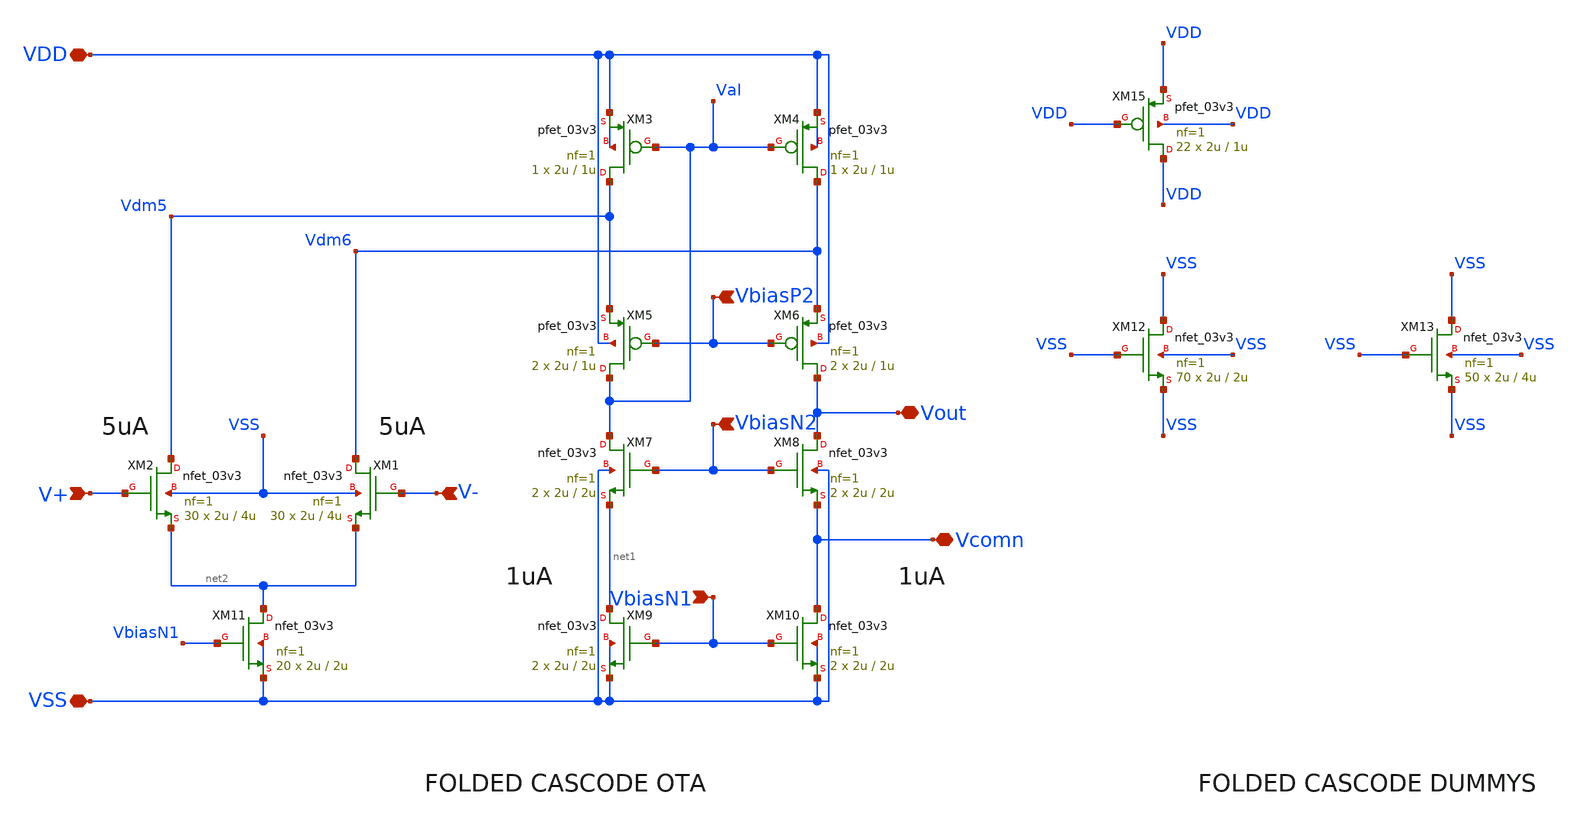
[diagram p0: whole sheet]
** sch_path: designs/libs/error_amplifier_N_input_core_v4/xschem/error_amplifier_N_input_core_v4.sch
**.subckt error_amplifier_N_input_core_v4 VbiasN2 VDD VbiasP2 VbiasN1 V+ V- VSS Vcomn Vout
*.ipin VbiasN2
*.iopin VDD
*.ipin VbiasP2
*.ipin VbiasN1
*.ipin V+
*.ipin V-
*.iopin VSS
*.iopin Vcomn
*.iopin Vout
XM4 Vdm6 Val VDD VDD pfet_03v3 L=1u W=2u nf=1 ad='int((nf+1)/2) * W/nf * 0.18u' as='int((nf+2)/2) * W/nf * 0.18u'
+ pd='2*int((nf+1)/2) * (W/nf + 0.18u)' ps='2*int((nf+2)/2) * (W/nf + 0.18u)' nrd='0.18u / W' nrs='0.18u / W'
+ sa=0 sb=0 sd=0 m=1
XM3 Vdm5 Val VDD VDD pfet_03v3 L=1u W=2u nf=1 ad='int((nf+1)/2) * W/nf * 0.18u' as='int((nf+2)/2) * W/nf * 0.18u'
+ pd='2*int((nf+1)/2) * (W/nf + 0.18u)' ps='2*int((nf+2)/2) * (W/nf + 0.18u)' nrd='0.18u / W' nrs='0.18u / W'
+ sa=0 sb=0 sd=0 m=1
XM5 Val VbiasP2 Vdm5 VDD pfet_03v3 L=1u W=2u nf=1 ad='int((nf+1)/2) * W/nf * 0.18u' as='int((nf+2)/2) * W/nf * 0.18u'
+ pd='2*int((nf+1)/2) * (W/nf + 0.18u)' ps='2*int((nf+2)/2) * (W/nf + 0.18u)' nrd='0.18u / W' nrs='0.18u / W'
+ sa=0 sb=0 sd=0 m=2
XM6 Vout VbiasP2 Vdm6 VDD pfet_03v3 L=1u W=2u nf=1 ad='int((nf+1)/2) * W/nf * 0.18u' as='int((nf+2)/2) * W/nf * 0.18u'
+ pd='2*int((nf+1)/2) * (W/nf + 0.18u)' ps='2*int((nf+2)/2) * (W/nf + 0.18u)' nrd='0.18u / W' nrs='0.18u / W'
+ sa=0 sb=0 sd=0 m=2
XM9 net1 VbiasN1 VSS VSS nfet_03v3 L=2u W=2u nf=1 ad='int((nf+1)/2) * W/nf * 0.18u' as='int((nf+2)/2) * W/nf * 0.18u'
+ pd='2*int((nf+1)/2) * (W/nf + 0.18u)' ps='2*int((nf+2)/2) * (W/nf + 0.18u)' nrd='0.18u / W' nrs='0.18u / W'
+ sa=0 sb=0 sd=0 m=2
XM8 Vout VbiasN2 Vcomn VSS nfet_03v3 L=2u W=2u nf=1 ad='int((nf+1)/2) * W/nf * 0.18u' as='int((nf+2)/2) * W/nf * 0.18u'
+ pd='2*int((nf+1)/2) * (W/nf + 0.18u)' ps='2*int((nf+2)/2) * (W/nf + 0.18u)' nrd='0.18u / W' nrs='0.18u / W'
+ sa=0 sb=0 sd=0 m=2
XM7 Val VbiasN2 net1 VSS nfet_03v3 L=2u W=2u nf=1 ad='int((nf+1)/2) * W/nf * 0.18u' as='int((nf+2)/2) * W/nf * 0.18u'
+ pd='2*int((nf+1)/2) * (W/nf + 0.18u)' ps='2*int((nf+2)/2) * (W/nf + 0.18u)' nrd='0.18u / W' nrs='0.18u / W'
+ sa=0 sb=0 sd=0 m=2
XM10 Vcomn VbiasN1 VSS VSS nfet_03v3 L=2u W=2u nf=1 ad='int((nf+1)/2) * W/nf * 0.18u' as='int((nf+2)/2) * W/nf * 0.18u'
+ pd='2*int((nf+1)/2) * (W/nf + 0.18u)' ps='2*int((nf+2)/2) * (W/nf + 0.18u)' nrd='0.18u / W' nrs='0.18u / W'
+ sa=0 sb=0 sd=0 m=2
XM15 VDD VDD VDD VDD pfet_03v3 L=1u W=2u nf=1 ad='int((nf+1)/2) * W/nf * 0.18u' as='int((nf+2)/2) * W/nf * 0.18u'
+ pd='2*int((nf+1)/2) * (W/nf + 0.18u)' ps='2*int((nf+2)/2) * (W/nf + 0.18u)' nrd='0.18u / W' nrs='0.18u / W'
+ sa=0 sb=0 sd=0 m=22
XM13 VSS VSS VSS VSS nfet_03v3 L=4u W=2u nf=1 ad='int((nf+1)/2) * W/nf * 0.18u' as='int((nf+2)/2) * W/nf * 0.18u'
+ pd='2*int((nf+1)/2) * (W/nf + 0.18u)' ps='2*int((nf+2)/2) * (W/nf + 0.18u)' nrd='0.18u / W' nrs='0.18u / W'
+ sa=0 sb=0 sd=0 m=50
XM12 VSS VSS VSS VSS nfet_03v3 L=2u W=2u nf=1 ad='int((nf+1)/2) * W/nf * 0.18u' as='int((nf+2)/2) * W/nf * 0.18u'
+ pd='2*int((nf+1)/2) * (W/nf + 0.18u)' ps='2*int((nf+2)/2) * (W/nf + 0.18u)' nrd='0.18u / W' nrs='0.18u / W'
+ sa=0 sb=0 sd=0 m=70
XM1 Vdm6 V- net2 VSS nfet_03v3 L=4u W=2u nf=1 ad='int((nf+1)/2) * W/nf * 0.18u' as='int((nf+2)/2) * W/nf * 0.18u'
+ pd='2*int((nf+1)/2) * (W/nf + 0.18u)' ps='2*int((nf+2)/2) * (W/nf + 0.18u)' nrd='0.18u / W' nrs='0.18u / W'
+ sa=0 sb=0 sd=0 m=30
XM2 Vdm5 V+ net2 VSS nfet_03v3 L=4u W=2u nf=1 ad='int((nf+1)/2) * W/nf * 0.18u' as='int((nf+2)/2) * W/nf * 0.18u'
+ pd='2*int((nf+1)/2) * (W/nf + 0.18u)' ps='2*int((nf+2)/2) * (W/nf + 0.18u)' nrd='0.18u / W' nrs='0.18u / W'
+ sa=0 sb=0 sd=0 m=30
XM11 net2 VbiasN1 VSS VSS nfet_03v3 L=2u W=2u nf=1 ad='int((nf+1)/2) * W/nf * 0.18u' as='int((nf+2)/2) * W/nf * 0.18u'
+ pd='2*int((nf+1)/2) * (W/nf + 0.18u)' ps='2*int((nf+2)/2) * (W/nf + 0.18u)' nrd='0.18u / W' nrs='0.18u / W'
+ sa=0 sb=0 sd=0 m=20
**.ends
.end
